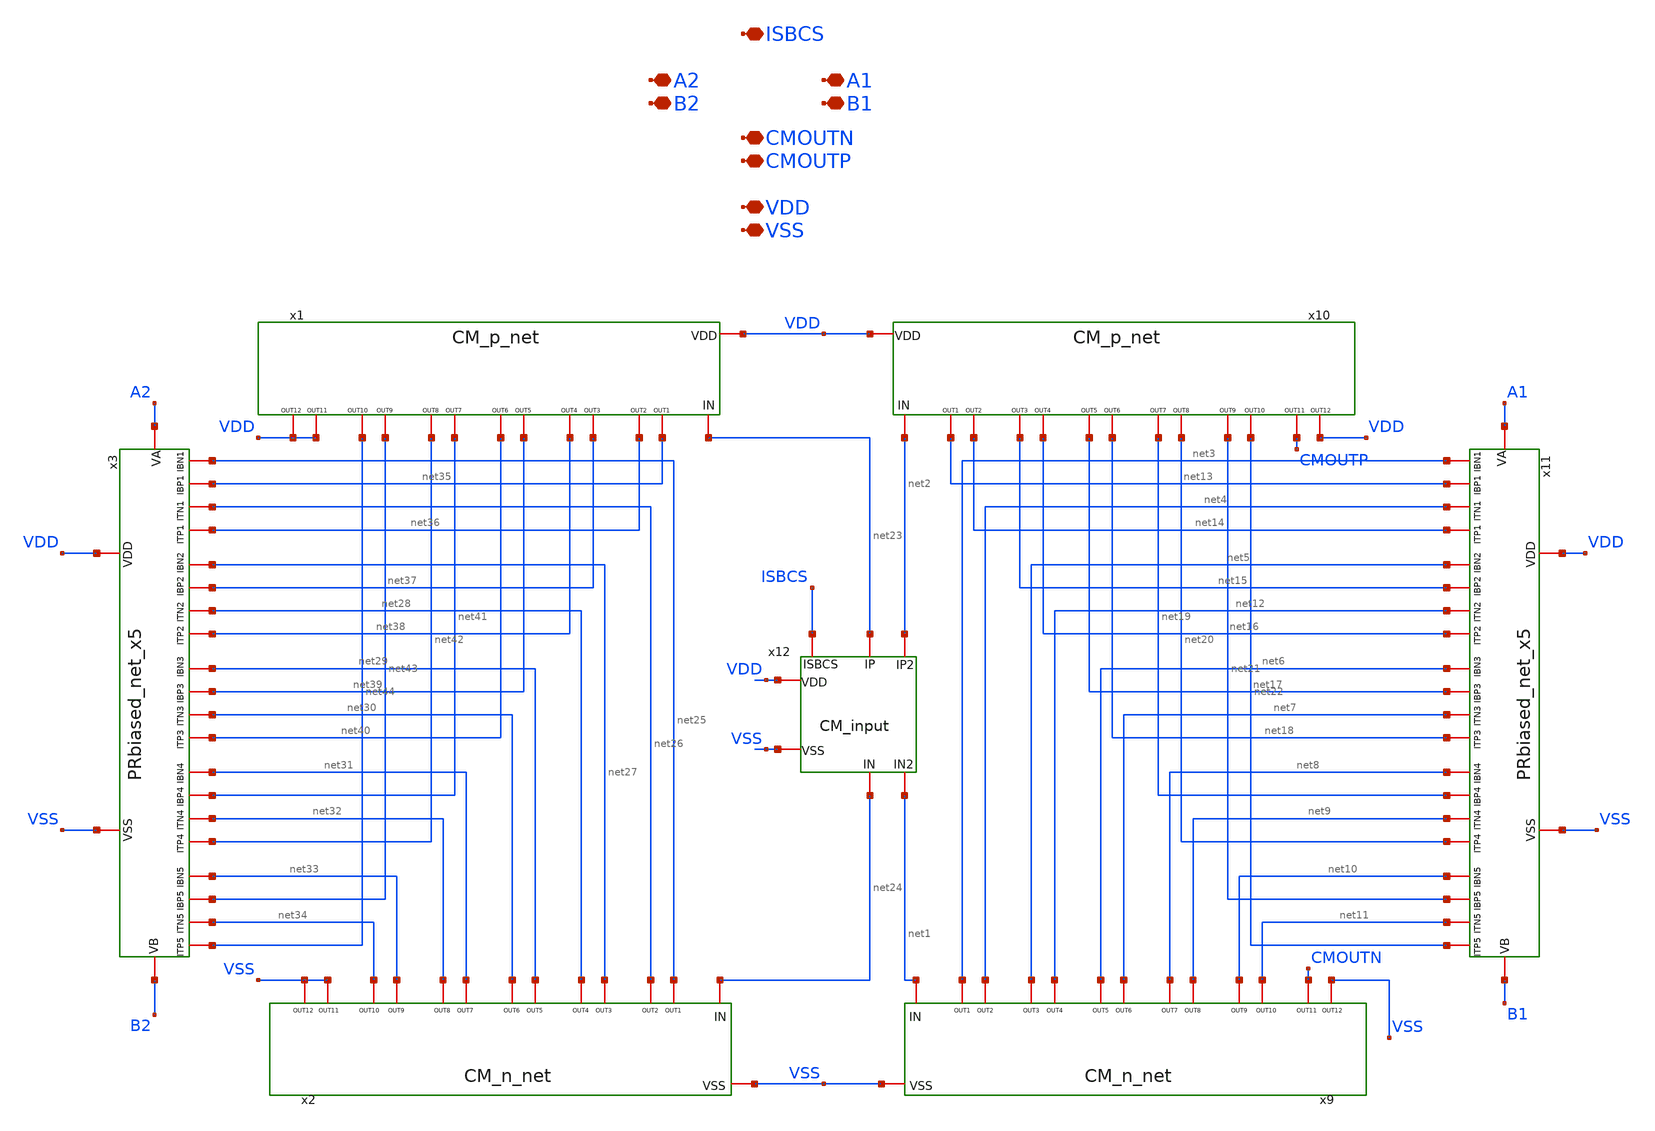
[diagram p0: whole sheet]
** sch_path: TIA_Filter/PR_CM_net.sch
**.subckt PR_CM_net ISBCS A2 B2 A1 B1 CMOUTN CMOUTP VDD VSS
*.iopin ISBCS
*.iopin A2
*.iopin B2
*.iopin A1
*.iopin B1
*.iopin CMOUTN
*.iopin CMOUTP
*.iopin VDD
*.iopin VSS
x9 net1 net3 net4 net5 net12 net6 net7 net8 net9 net10 net11 CMOUTN VSS VSS CM_n_net
x10 net2 net13 net14 net15 net16 net17 net18 net19 net20 net21 net22 CMOUTP VDD VDD CM_p_net
x11 A1 B1 net6 net5 net3 net10 net8 net17 net15 net19 net13 net21 net7 net4 net11 net12 net9 net22
+ net16 net14 net20 net18 VDD VSS PRbiased_net_x5
x12 net23 net2 net24 net1 ISBCS VDD VSS CM_input
x1 net23 net35 net36 net37 net38 net39 net40 net41 net42 net43 net44 VDD VDD VDD CM_p_net
x2 net24 net25 net26 net27 net28 net29 net30 net31 net32 net33 net34 VSS VSS VSS CM_n_net
x3 A2 B2 net29 net27 net25 net33 net31 net39 net37 net41 net35 net43 net30 net26 net34 net28 net32
+ net44 net38 net36 net42 net40 VDD VSS PRbiased_net_x5
**.ends
.end
